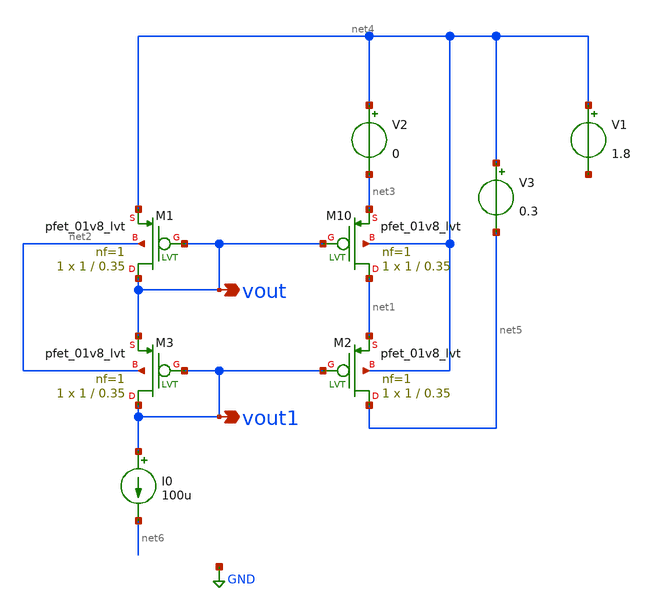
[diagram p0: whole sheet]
** sch_path: xschem/cascade_pmos.sch
**.subckt cascade_pmos vout vout1
*.opin vout
*.opin vout1
XM10 net1 vout net3 net4 sky130_fd_pr__pfet_01v8_lvt L=0.35 W=1 nf=1 ad='int((1 + 1)/2) * 1 / 1 * 0.29'
+ as='int((1 + 2)/2) * 1 / 1 * 0.29' pd='2*int((1 + 1)/2) * (1 / 1 + 0.29)' ps='2*int((1 + 2)/2) * (1 / 1 + 0.29)'
+ nrd='0.29 / 1 ' nrs='0.29 / 1 ' sa=0 sb=0 sd=0 mult=1 m=1
XM1 vout vout net4 net2 sky130_fd_pr__pfet_01v8_lvt L=0.35 W=1 nf=1 ad='int((1 + 1)/2) * 1 / 1 * 0.29'
+ as='int((1 + 2)/2) * 1 / 1 * 0.29' pd='2*int((1 + 1)/2) * (1 / 1 + 0.29)' ps='2*int((1 + 2)/2) * (1 / 1 + 0.29)'
+ nrd='0.29 / 1 ' nrs='0.29 / 1 ' sa=0 sb=0 sd=0 mult=1 m=1
XM2 net5 vout1 net1 net4 sky130_fd_pr__pfet_01v8_lvt L=0.35 W=1 nf=1 ad='int((1 + 1)/2) * 1 / 1 * 0.29'
+ as='int((1 + 2)/2) * 1 / 1 * 0.29' pd='2*int((1 + 1)/2) * (1 / 1 + 0.29)' ps='2*int((1 + 2)/2) * (1 / 1 + 0.29)'
+ nrd='0.29 / 1 ' nrs='0.29 / 1 ' sa=0 sb=0 sd=0 mult=1 m=1
XM3 vout1 vout1 vout net2 sky130_fd_pr__pfet_01v8_lvt L=0.35 W=1 nf=1 ad='int((1 + 1)/2) * 1 / 1 * 0.29'
+ as='int((1 + 2)/2) * 1 / 1 * 0.29' pd='2*int((1 + 1)/2) * (1 / 1 + 0.29)' ps='2*int((1 + 2)/2) * (1 / 1 + 0.29)'
+ nrd='0.29 / 1 ' nrs='0.29 / 1 ' sa=0 sb=0 sd=0 mult=1 m=1
I0 vout1 net6 100u
V2 net4 net3 0
V3 net4 net5 0.3
V1 net4 net7 1.8
**.ends
.GLOBAL GND
.end
